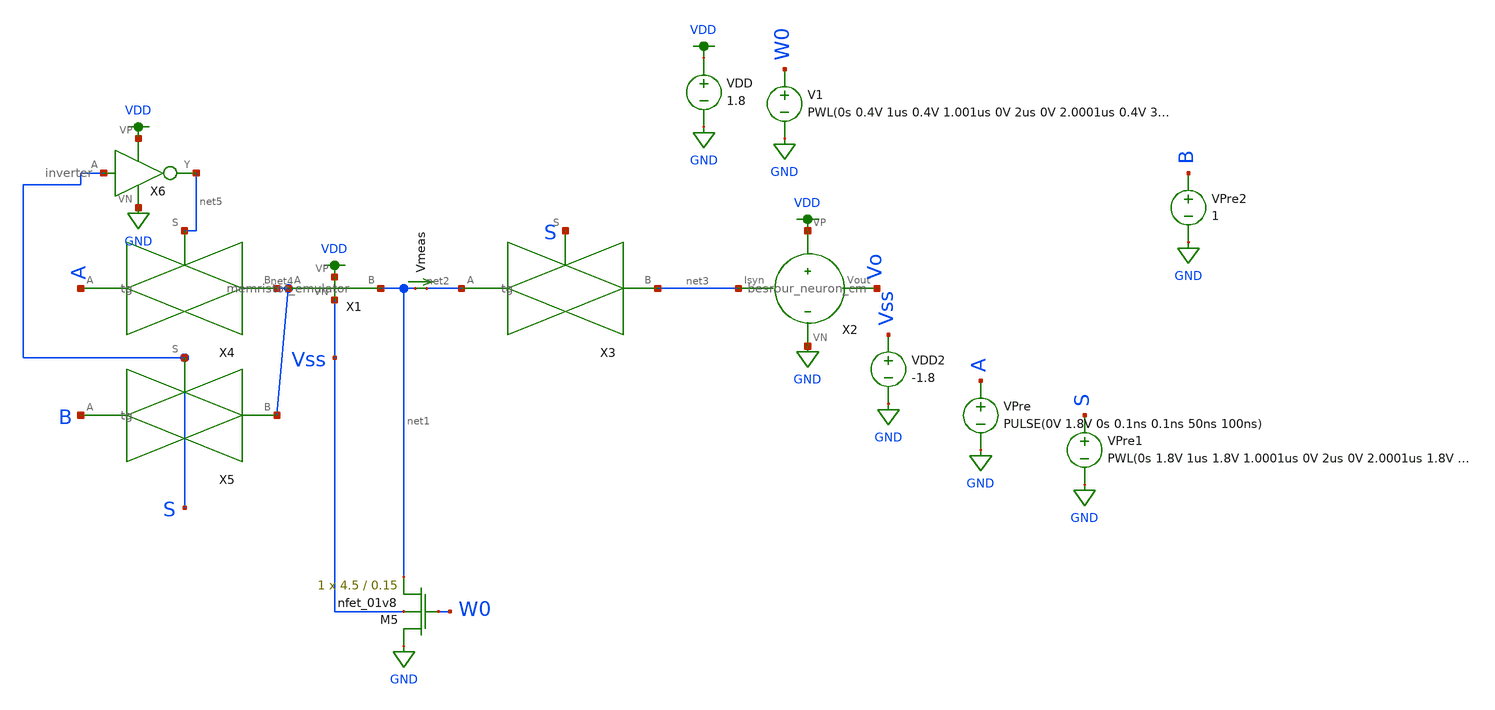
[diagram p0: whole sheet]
** sch_path: schematic/tran_memristor_emulator_training.sch
**.subckt tran_memristor_emulator_training
VDD VDD GND 1.8
V1 W0 GND PWL(0s 0.4V 1us 0.4V 1.001us 0V 2us 0V 2.0001us 0.4V 3us 0.4V)
VPre A GND PULSE(0V 1.8V 0s 0.1ns 0.1ns 50ns 100ns)

X1 VDD Vss net1 net4 memristor_emulator
VDD2 Vss GND -1.8
Vmeas net1 net2 0
.save i(vmeas)
XM5 GND W0 net1 Vss sky130_fd_pr__nfet_01v8 L=0.15 W=4.5 nf=1 ad='int((nf+1)/2) * W/nf * 0.29' as='int((nf+2)/2) * W/nf * 0.29'
+ pd='2*int((nf+1)/2) * (W/nf + 0.29)' ps='2*int((nf+2)/2) * (W/nf + 0.29)' nrd='0.29 / W' nrs='0.29 / W'
+ sa=0 sb=0 sd=0 mult=1 m=1
X2 net3 Vo VDD GND besrour_neuron_cm
X3 S net2 net3 tg
VPre1 S GND PWL(0s 1.8V 1us 1.8V 1.0001us 0V 2us 0V 2.0001us 1.8V 3us 1.8V)
X4 net5 A net4 tg
X5 S B net4 tg
X6 S GND VDD net5 inverter
VPre2 B GND 1
**** begin user architecture code

.param W=2
.param L=0.3
.tran 1n 10u
.save all



.option wnflag=1
.param MC_SWITCH=0.0
.lib ~/skywater/skywater-pdk/libraries/sky130_fd_pr_ngspice/latest/models/sky130.lib.spice tt

**** end user architecture code
**.ends

* expanding   symbol:  /home/madvlsi/neuromorphic_computing_final/schematic/memristor_emulator.sym #
*+ of pins=4
** sym_path: schematic/memristor_emulator.sym
** sch_path: schematic/memristor_emulator.sch
.subckt memristor_emulator VP VN B A
*.iopin VN
*.iopin VP
*.iopin B
*.iopin A
XM1 B net1 A B sky130_fd_pr__pfet_01v8 L=0.5 W=12 nf=1 ad='int((nf+1)/2) * W/nf * 0.29' as='int((nf+2)/2) * W/nf * 0.29'
+ pd='2*int((nf+1)/2) * (W/nf + 0.29)' ps='2*int((nf+2)/2) * (W/nf + 0.29)' nrd='0.29 / W' nrs='0.29 / W'
+ sa=0 sb=0 sd=0 mult=1 m=1
XM2 VP A net1 VP sky130_fd_pr__pfet_01v8 L=2 W=3 nf=1 ad='int((nf+1)/2) * W/nf * 0.29' as='int((nf+2)/2) * W/nf * 0.29'
+ pd='2*int((nf+1)/2) * (W/nf + 0.29)' ps='2*int((nf+2)/2) * (W/nf + 0.29)' nrd='0.29 / W' nrs='0.29 / W'
+ sa=0 sb=0 sd=0 mult=1 m=1
XM3 VN net1 VN VN sky130_fd_pr__nfet_01v8 L=20 W=20 nf=1 ad='int((nf+1)/2) * W/nf * 0.29' as='int((nf+2)/2) * W/nf * 0.29'
+ pd='2*int((nf+1)/2) * (W/nf + 0.29)' ps='2*int((nf+2)/2) * (W/nf + 0.29)' nrd='0.29 / W' nrs='0.29 / W'
+ sa=0 sb=0 sd=0 mult=1 m=1
XM4 VN B net1 VN sky130_fd_pr__nfet_01v8 L=3 W=2 nf=1 ad='int((nf+1)/2) * W/nf * 0.29' as='int((nf+2)/2) * W/nf * 0.29'
+ pd='2*int((nf+1)/2) * (W/nf + 0.29)' ps='2*int((nf+2)/2) * (W/nf + 0.29)' nrd='0.29 / W' nrs='0.29 / W'
+ sa=0 sb=0 sd=0 mult=1 m=1
.ends


* expanding   symbol:  /home/madvlsi/neuromorphic_computing_final/schematic/besrour_neuron_cm.sym #
*+ of pins=4
** sym_path: schematic/besrour_neuron_cm.sym
** sch_path: schematic/besrour_neuron_cm.sch
.subckt besrour_neuron_cm Isyn Vout VP VN
*.iopin VP
*.iopin VN
*.iopin Isyn
*.opin Vout
XM2 VMEMINT net1 VP VDD sky130_fd_pr__pfet_01v8 L={L} W={W} nf=1 ad='int((nf+1)/2) * W/nf * 0.29' as='int((nf+2)/2) * W/nf * 0.29'
+ pd='2*int((nf+1)/2) * (W/nf + 0.29)' ps='2*int((nf+2)/2) * (W/nf + 0.29)' nrd='0.29 / W' nrs='0.29 / W'
+ sa=0 sb=0 sd=0 mult=1 m=1
XM3 VP net3 VMEMINT VDD sky130_fd_pr__pfet_01v8 L={L} W={W} nf=1 ad='int((nf+1)/2) * W/nf * 0.29' as='int((nf+2)/2) * W/nf * 0.29'
+ pd='2*int((nf+1)/2) * (W/nf + 0.29)' ps='2*int((nf+2)/2) * (W/nf + 0.29)' nrd='0.29 / W' nrs='0.29 / W'
+ sa=0 sb=0 sd=0 mult=1 m=1
XM4 net3 VMEMINT VP VDD sky130_fd_pr__pfet_01v8 L={L} W={W} nf=1 ad='int((nf+1)/2) * W/nf * 0.29' as='int((nf+2)/2) * W/nf * 0.29'
+ pd='2*int((nf+1)/2) * (W/nf + 0.29)' ps='2*int((nf+2)/2) * (W/nf + 0.29)' nrd='0.29 / W' nrs='0.29 / W'
+ sa=0 sb=0 sd=0 mult=1 m=1
XM5 net2 net3 VP VDD sky130_fd_pr__pfet_01v8 L={L} W={W} nf=1 ad='int((nf+1)/2) * W/nf * 0.29' as='int((nf+2)/2) * W/nf * 0.29'
+ pd='2*int((nf+1)/2) * (W/nf + 0.29)' ps='2*int((nf+2)/2) * (W/nf + 0.29)' nrd='0.29 / W' nrs='0.29 / W'
+ sa=0 sb=0 sd=0 mult=1 m=1
XM6 net3 VMEMINT VN GND sky130_fd_pr__nfet_01v8 L={L} W={W} nf=1 ad='int((nf+1)/2) * W/nf * 0.29' as='int((nf+2)/2) * W/nf * 0.29'
+ pd='2*int((nf+1)/2) * (W/nf + 0.29)' ps='2*int((nf+2)/2) * (W/nf + 0.29)' nrd='0.29 / W' nrs='0.29 / W'
+ sa=0 sb=0 sd=0 mult=1 m=1
XM8 net2 net3 VN GND sky130_fd_pr__nfet_01v8 L={L} W={W} nf=1 ad='int((nf+1)/2) * W/nf * 0.29' as='int((nf+2)/2) * W/nf * 0.29'
+ pd='2*int((nf+1)/2) * (W/nf + 0.29)' ps='2*int((nf+2)/2) * (W/nf + 0.29)' nrd='0.29 / W' nrs='0.29 / W'
+ sa=0 sb=0 sd=0 mult=1 m=1
C1 VMEMINT VN 340f m=1
C2 net2 VN 340f m=1
XM9 net4 net2 VP VDD sky130_fd_pr__pfet_01v8 L={L} W={W} nf=1 ad='int((nf+1)/2) * W/nf * 0.29' as='int((nf+2)/2) * W/nf * 0.29'
+ pd='2*int((nf+1)/2) * (W/nf + 0.29)' ps='2*int((nf+2)/2) * (W/nf + 0.29)' nrd='0.29 / W' nrs='0.29 / W'
+ sa=0 sb=0 sd=0 mult=1 m=1
XM10 net4 net2 VN GND sky130_fd_pr__nfet_01v8 L={L} W={W} nf=1 ad='int((nf+1)/2) * W/nf * 0.29' as='int((nf+2)/2) * W/nf * 0.29'
+ pd='2*int((nf+1)/2) * (W/nf + 0.29)' ps='2*int((nf+2)/2) * (W/nf + 0.29)' nrd='0.29 / W' nrs='0.29 / W'
+ sa=0 sb=0 sd=0 mult=1 m=1
XM11 Vout net4 VP VDD sky130_fd_pr__pfet_01v8 L={L} W={W} nf=1 ad='int((nf+1)/2) * W/nf * 0.29' as='int((nf+2)/2) * W/nf * 0.29'
+ pd='2*int((nf+1)/2) * (W/nf + 0.29)' ps='2*int((nf+2)/2) * (W/nf + 0.29)' nrd='0.29 / W' nrs='0.29 / W'
+ sa=0 sb=0 sd=0 mult=1 m=1
XM12 Vout net4 VN GND sky130_fd_pr__nfet_01v8 L={L} W={W} nf=1 ad='int((nf+1)/2) * W/nf * 0.29' as='int((nf+2)/2) * W/nf * 0.29'
+ pd='2*int((nf+1)/2) * (W/nf + 0.29)' ps='2*int((nf+2)/2) * (W/nf + 0.29)' nrd='0.29 / W' nrs='0.29 / W'
+ sa=0 sb=0 sd=0 mult=1 m=1
XM13 net1 Isyn VN GND sky130_fd_pr__nfet_01v8 L={L} W={W} nf=1 ad='int((nf+1)/2) * W/nf * 0.29' as='int((nf+2)/2) * W/nf * 0.29'
+ pd='2*int((nf+1)/2) * (W/nf + 0.29)' ps='2*int((nf+2)/2) * (W/nf + 0.29)' nrd='0.29 / W' nrs='0.29 / W'
+ sa=0 sb=0 sd=0 mult=1 m=1
XM14 VN Isyn Isyn GND sky130_fd_pr__nfet_01v8 L={L} W={W} nf=1 ad='int((nf+1)/2) * W/nf * 0.29' as='int((nf+2)/2) * W/nf * 0.29'
+ pd='2*int((nf+1)/2) * (W/nf + 0.29)' ps='2*int((nf+2)/2) * (W/nf + 0.29)' nrd='0.29 / W' nrs='0.29 / W'
+ sa=0 sb=0 sd=0 mult=1 m=1
XM1 VP net1 net1 VDD sky130_fd_pr__pfet_01v8 L={L} W={W} nf=1 ad='int((nf+1)/2) * W/nf * 0.29' as='int((nf+2)/2) * W/nf * 0.29'
+ pd='2*int((nf+1)/2) * (W/nf + 0.29)' ps='2*int((nf+2)/2) * (W/nf + 0.29)' nrd='0.29 / W' nrs='0.29 / W'
+ sa=0 sb=0 sd=0 mult=1 m=1
XM7 VN net2 VMEMINT GND sky130_fd_pr__nfet_01v8 L={L} W={W} nf=1 ad='int((nf+1)/2) * W/nf * 0.29' as='int((nf+2)/2) * W/nf * 0.29'
+ pd='2*int((nf+1)/2) * (W/nf + 0.29)' ps='2*int((nf+2)/2) * (W/nf + 0.29)' nrd='0.29 / W' nrs='0.29 / W'
+ sa=0 sb=0 sd=0 mult=1 m=1
.ends


* expanding   symbol:  /home/madvlsi/neuromorphic_computing_final/schematic/tg.sym # of pins=3
** sym_path: schematic/tg.sym
** sch_path: schematic/tg.sch
.subckt tg S A B
*.ipin S
*.iopin B
*.iopin A
X1 S GND VDD net1 inverter
XM1 B net1 A VDD sky130_fd_pr__pfet_01v8 L=0.3 W=6 nf=1 ad='int((nf+1)/2) * W/nf * 0.29' as='int((nf+2)/2) * W/nf * 0.29'
+ pd='2*int((nf+1)/2) * (W/nf + 0.29)' ps='2*int((nf+2)/2) * (W/nf + 0.29)' nrd='0.29 / W' nrs='0.29 / W'
+ sa=0 sb=0 sd=0 mult=1 m=1
XM2 B S A GND sky130_fd_pr__nfet_01v8 L=0.3 W=6 nf=1 ad='int((nf+1)/2) * W/nf * 0.29' as='int((nf+2)/2) * W/nf * 0.29'
+ pd='2*int((nf+1)/2) * (W/nf + 0.29)' ps='2*int((nf+2)/2) * (W/nf + 0.29)' nrd='0.29 / W' nrs='0.29 / W'
+ sa=0 sb=0 sd=0 mult=1 m=1
.ends


* expanding   symbol:  /home/madvlsi/neuromorphic_computing_final/schematic/inverter.sym # of pins=4
** sym_path: schematic/inverter.sym
** sch_path: schematic/inverter.sch
.subckt inverter A VN VP Y
*.ipin A
*.iopin VP
*.iopin VN
*.opin Y
XM1 Y A VN VN sky130_fd_pr__nfet_01v8 L=0.15 W=1 nf=1 ad='int((nf+1)/2) * W/nf * 0.29' as='int((nf+2)/2) * W/nf * 0.29'
+ pd='2*int((nf+1)/2) * (W/nf + 0.29)' ps='2*int((nf+2)/2) * (W/nf + 0.29)' nrd='0.29 / W' nrs='0.29 / W'
+ sa=0 sb=0 sd=0 mult=1 m=1
XM2 Y A VP VP sky130_fd_pr__pfet_01v8 L=0.15 W=1 nf=1 ad='int((nf+1)/2) * W/nf * 0.29' as='int((nf+2)/2) * W/nf * 0.29'
+ pd='2*int((nf+1)/2) * (W/nf + 0.29)' ps='2*int((nf+2)/2) * (W/nf + 0.29)' nrd='0.29 / W' nrs='0.29 / W'
+ sa=0 sb=0 sd=0 mult=1 m=1
.ends

.GLOBAL GND
.GLOBAL VDD
.end
